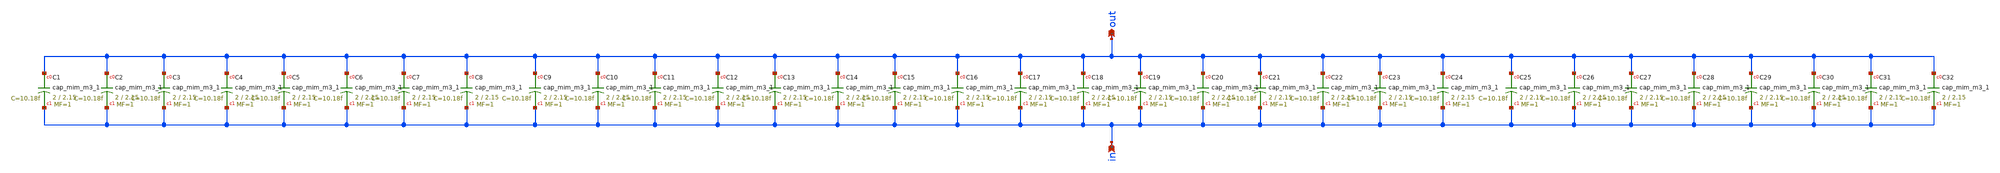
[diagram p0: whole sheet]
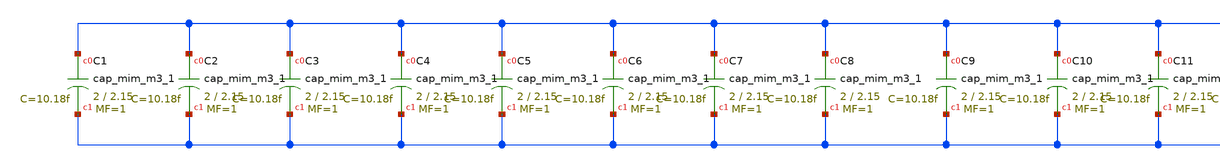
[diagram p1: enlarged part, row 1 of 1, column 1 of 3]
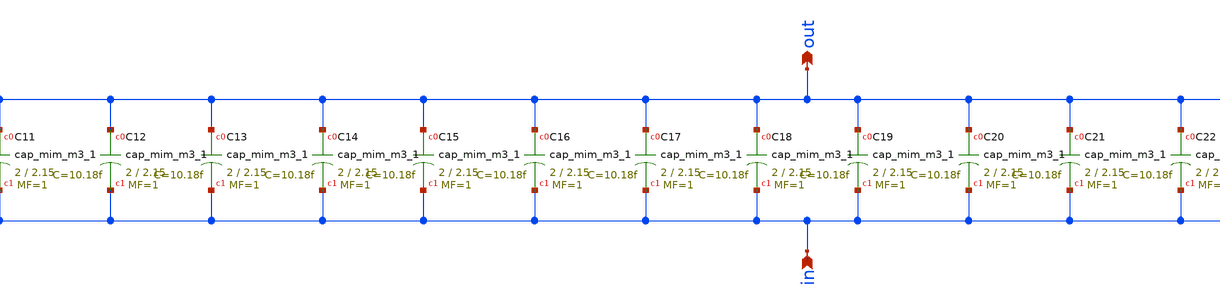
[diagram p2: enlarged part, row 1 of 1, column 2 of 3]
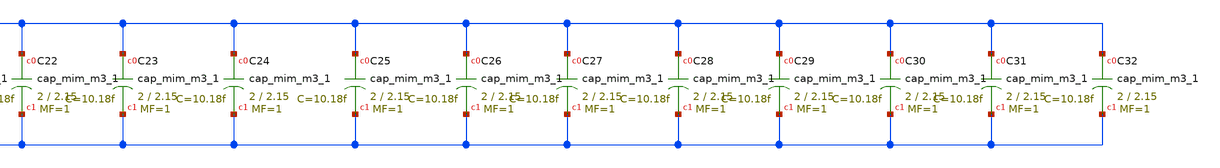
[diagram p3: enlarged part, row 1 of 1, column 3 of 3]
** sch_path: xschem/cap32.sch
**.subckt cap32 in out
*.ipin in
*.opin out
XC1 out in sky130_fd_pr__cap_mim_m3_1 W=2 L=2.15 MF=1 m=1
XC2 out in sky130_fd_pr__cap_mim_m3_1 W=2 L=2.15 MF=1 m=1
XC3 out in sky130_fd_pr__cap_mim_m3_1 W=2 L=2.15 MF=1 m=1
XC4 out in sky130_fd_pr__cap_mim_m3_1 W=2 L=2.15 MF=1 m=1
XC5 out in sky130_fd_pr__cap_mim_m3_1 W=2 L=2.15 MF=1 m=1
XC6 out in sky130_fd_pr__cap_mim_m3_1 W=2 L=2.15 MF=1 m=1
XC7 out in sky130_fd_pr__cap_mim_m3_1 W=2 L=2.15 MF=1 m=1
XC8 out in sky130_fd_pr__cap_mim_m3_1 W=2 L=2.15 MF=1 m=1
XC9 out in sky130_fd_pr__cap_mim_m3_1 W=2 L=2.15 MF=1 m=1
XC10 out in sky130_fd_pr__cap_mim_m3_1 W=2 L=2.15 MF=1 m=1
XC11 out in sky130_fd_pr__cap_mim_m3_1 W=2 L=2.15 MF=1 m=1
XC12 out in sky130_fd_pr__cap_mim_m3_1 W=2 L=2.15 MF=1 m=1
XC13 out in sky130_fd_pr__cap_mim_m3_1 W=2 L=2.15 MF=1 m=1
XC14 out in sky130_fd_pr__cap_mim_m3_1 W=2 L=2.15 MF=1 m=1
XC15 out in sky130_fd_pr__cap_mim_m3_1 W=2 L=2.15 MF=1 m=1
XC16 out in sky130_fd_pr__cap_mim_m3_1 W=2 L=2.15 MF=1 m=1
XC17 out in sky130_fd_pr__cap_mim_m3_1 W=2 L=2.15 MF=1 m=1
XC18 out in sky130_fd_pr__cap_mim_m3_1 W=2 L=2.15 MF=1 m=1
XC19 out in sky130_fd_pr__cap_mim_m3_1 W=2 L=2.15 MF=1 m=1
XC20 out in sky130_fd_pr__cap_mim_m3_1 W=2 L=2.15 MF=1 m=1
XC21 out in sky130_fd_pr__cap_mim_m3_1 W=2 L=2.15 MF=1 m=1
XC22 out in sky130_fd_pr__cap_mim_m3_1 W=2 L=2.15 MF=1 m=1
XC23 out in sky130_fd_pr__cap_mim_m3_1 W=2 L=2.15 MF=1 m=1
XC24 out in sky130_fd_pr__cap_mim_m3_1 W=2 L=2.15 MF=1 m=1
XC25 out in sky130_fd_pr__cap_mim_m3_1 W=2 L=2.15 MF=1 m=1
XC26 out in sky130_fd_pr__cap_mim_m3_1 W=2 L=2.15 MF=1 m=1
XC27 out in sky130_fd_pr__cap_mim_m3_1 W=2 L=2.15 MF=1 m=1
XC28 out in sky130_fd_pr__cap_mim_m3_1 W=2 L=2.15 MF=1 m=1
XC29 out in sky130_fd_pr__cap_mim_m3_1 W=2 L=2.15 MF=1 m=1
XC30 out in sky130_fd_pr__cap_mim_m3_1 W=2 L=2.15 MF=1 m=1
XC31 out in sky130_fd_pr__cap_mim_m3_1 W=2 L=2.15 MF=1 m=1
XC32 out in sky130_fd_pr__cap_mim_m3_1 W=2 L=2.15 MF=1 m=1
**.ends
.end
